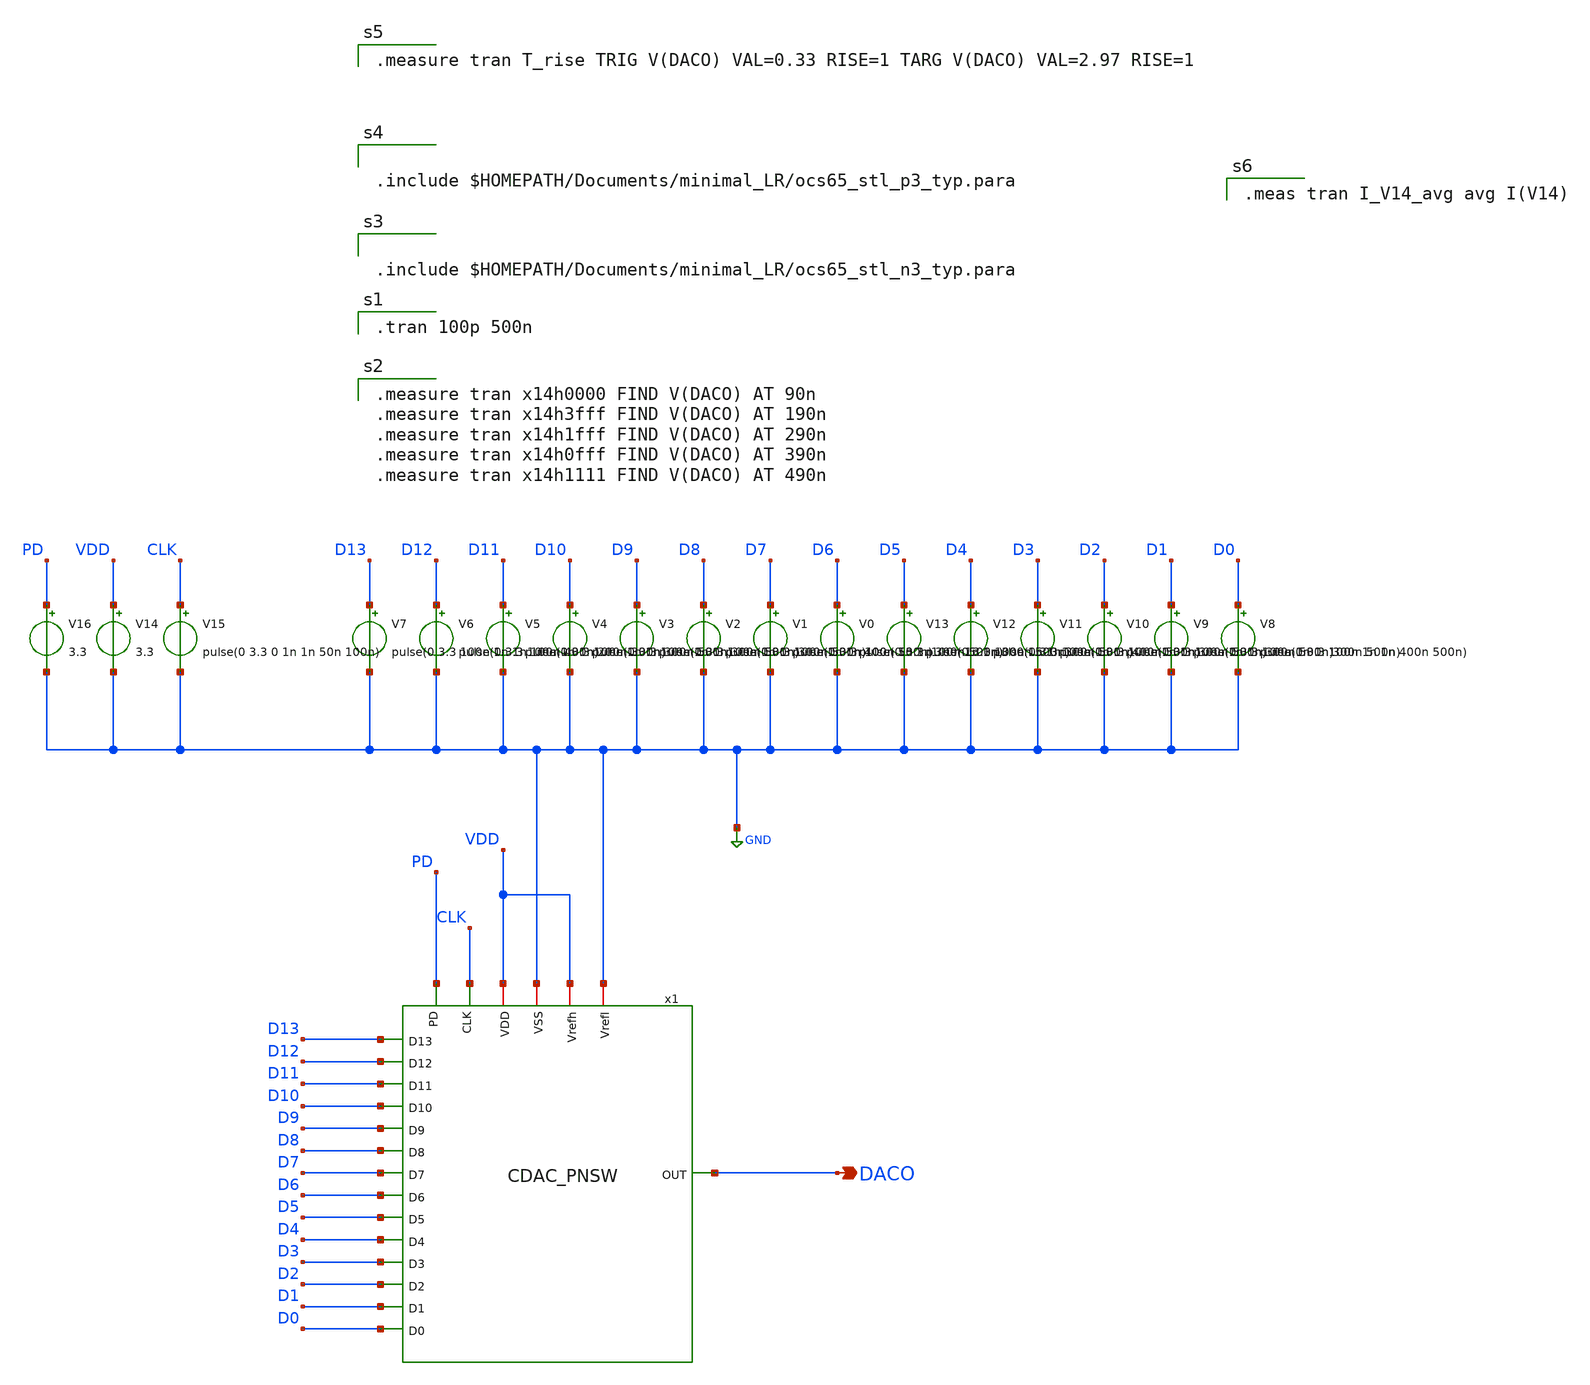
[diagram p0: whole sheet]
** sch_path: CDAC_sim.sch
**.subckt CDAC_sim DACO
*.opin DACO
V14 VDD GND 3.3
V15 CLK GND pulse(0 3.3 0 1n 1n 50n 100n)
V16 PD GND 3.3
V13 D5 GND pulse(0 3.3 100n 1n 1n 300n 500n)
V12 D4 GND pulse(0 3.3 100n 1n 1n 400n 500n)
V11 D3 GND pulse(0 3.3 100n 1n 1n 300n 500n)
V10 D2 GND pulse(0 3.3 100n 1n 1n 300n 500n)
V9 D1 GND pulse(0 3.3 100n 1n 1n 300n 500n)
V8 D0 GND pulse(0 3.3 100n 1n 1n 400n 500n)
V7 D13 GND pulse(0 3.3 100n 1n 1n 100n 400n)
V6 D12 GND pulse(0 3.3 100n 1n 1n 200n 300n)
V5 D11 GND pulse(0 3.3 100n 1n 1n 300n 500n)
V4 D10 GND pulse(0 3.3 100n 1n 1n 300n 500n)
V3 D9 GND pulse(0 3.3 100n 1n 1n 300n 500n)
V2 D8 GND pulse(0 3.3 100n 1n 1n 400n 500n)
V1 D7 GND pulse(0 3.3 100n 1n 1n 300n 500n)
V0 D6 GND pulse(0 3.3 100n 1n 1n 300n 500n)
x1 CLK D11 D13 D12 D7 D10 D1 D0 D9 D8 D2 D6 D5 D4 D3 DACO GND VDD GND VDD PD CDAC_PNSW
**** begin user architecture code

.tran 100p 500n


.measure tran x14h0000 FIND V(DACO) AT 90n
.measure tran x14h3fff FIND V(DACO) AT 190n
.measure tran x14h1fff FIND V(DACO) AT 290n
.measure tran x14h0fff FIND V(DACO) AT 390n
.measure tran x14h1111 FIND V(DACO) AT 490n



.include $HOMEPATH/Documents/minimal_LR/ocs65_stl_n3_typ.para



.include $HOMEPATH/Documents/minimal_LR/ocs65_stl_p3_typ.para


.measure tran T_rise TRIG V(DACO) VAL=0.33 RISE=1 TARG V(DACO) VAL=2.97 RISE=1


.meas tran I_V14_avg avg I(V14)

**** end user architecture code
**.ends

* expanding   symbol:  CDAC_PNSW.sym # of pins=21
** sym_path: CDAC_PNSW.sym
** sch_path: CDAC_PNSW.sch
.subckt CDAC_PNSW CLK D11 D13 D12 D7 D10 D1 D0 D9 D8 D2 D6 D5 D4 D3 OUT VSS VDD Vrefl Vrefh PD
*.opin OUT
*.iopin Vrefh
*.iopin Vrefl
*.ipin D13
*.ipin D12
*.ipin D11
*.ipin D10
*.iopin VSS
*.iopin VDD
*.ipin D9
*.ipin D8
*.ipin D7
*.ipin D6
*.ipin D5
*.ipin D4
*.ipin D3
*.ipin D2
*.ipin D1
*.ipin D0
*.ipin CLK
*.ipin PD
C1 OUT Vrefl 33f m=1
C2 OUT net1 33f m=1
C3 OUT net2 66f m=1
C4 OUT net4 132f m=1
C5 OUT net3 264f m=1
x15 VDD D13b D13 VSS INV
x16 VDD D12b D12 VSS INV
x17 VDD D11b D11 VSS INV
x18 VDD D10b D10 VSS INV
C6 OUT net5 528f m=1
C7 OUT net6 1.056p m=1
C8 OUT net8 2.112p m=1
C9 OUT net7 4.224p m=1
C10 OUT net10 8.448p m=1
C11 OUT net9 16.896p m=1
C12 OUT net11 33.792p m=1
C13 OUT net12 67.584p m=1
C14 OUT net14 135.168p m=1
C15 OUT net13 270.336p m=1
x34 VDD D9b D9 VSS INV
x35 VDD D8b D8 VSS INV
x36 VDD D7b D7 VSS INV
x37 VDD D6b D6 VSS INV
x38 VDD D5b D5 VSS INV
x39 VDD D4b D4 VSS INV
x40 VDD D3b D3 VSS INV
x41 VDD D2b D2 VSS INV
x42 VDD D1b D1 VSS INV
x43 VDD D0b D0 VSS INV
x72 VDD CLK CLK1 VSS net15 NOL
x31 D13bO VSS net13 Vrefl NMOSSW16
x33 D12bO VSS net14 Vrefl NMOSSW8
x29 D11bO VSS net12 Vrefl NMOSSW4
x27 D10bO VSS net11 Vrefl NMOSSW2
x1 resetPD VSS OUT Vrefl NMOSSW16
x2 D0bO VSS net1 Vrefl NMOSSW
x4 D1bO VSS net2 Vrefl NMOSSW
x6 D2bO VSS net4 Vrefl NMOSSW
x8 D3bO VSS net3 Vrefl NMOSSW
x10 D4bO VSS net5 Vrefl NMOSSW
x12 D5bO VSS net6 Vrefl NMOSSW
x14 D6bO VSS net8 Vrefl NMOSSW
x20 D7bO VSS net7 Vrefl NMOSSW
x22 D8bO VSS net10 Vrefl NMOSSW
x24 D9bO VSS net9 Vrefl NMOSSW
x3 D13A net13 Vrefh VDD PMOSSW16
x5 D12A net14 Vrefh VDD PMOSSW8
x7 D11A net12 Vrefh VDD PMOSSW4
x9 D10A net11 Vrefh VDD PMOSSW2
x11 D9A net9 Vrefh VDD PMOSSW
x13 D8A net10 Vrefh VDD PMOSSW
x19 D7A net7 Vrefh VDD PMOSSW
x21 D6A net8 Vrefh VDD PMOSSW
x23 D5A net6 Vrefh VDD PMOSSW
x25 D4A net5 Vrefh VDD PMOSSW
x26 D3A net3 Vrefh VDD PMOSSW
x28 D2A net4 Vrefh VDD PMOSSW
x30 D1A net2 Vrefh VDD PMOSSW
x32 D0A net1 Vrefh VDD PMOSSW
x73 VDD CLK2 net15 VSS INV
x74 VDD net16 PD VSS INV
x75 VDD net17 resetPD net16 VSS OR
x44 VDD D13A CLK1 D13b VSS IMPLY
x45 VDD D12A CLK1 D12b VSS IMPLY
x46 VDD D11A CLK1 D11b VSS IMPLY
x47 VDD D10A CLK1 D10b VSS IMPLY
x48 VDD D9A CLK1 D9b VSS IMPLY
x49 VDD D8A CLK1 D8b VSS IMPLY
x50 VDD D7A CLK1 D7b VSS IMPLY
x51 VDD D6A CLK1 D6b VSS IMPLY
x52 VDD D5A CLK1 D5b VSS IMPLY
x53 VDD D4A CLK1 D4b VSS IMPLY
x54 VDD D3A CLK1 D3b VSS IMPLY
x55 VDD D2A CLK1 D2b VSS IMPLY
x56 VDD D1A CLK1 D1b VSS IMPLY
x57 VDD D0A CLK1 D0b VSS IMPLY
x58 VDD D0bO CLK2 D0b VSS IMPLY
x59 VDD D1bO CLK2 D1b VSS IMPLY
x60 VDD D2bO CLK2 D2b VSS IMPLY
x61 VDD D3bO CLK2 D3b VSS IMPLY
x62 VDD D4bO CLK2 D4b VSS IMPLY
x63 VDD D5bO CLK2 D5b VSS IMPLY
x64 VDD D6bO CLK2 D6b VSS IMPLY
x65 VDD D7bO CLK2 D7b VSS IMPLY
x66 VDD D8bO CLK2 D8b VSS IMPLY
x67 VDD D9bO CLK2 D9b VSS IMPLY
x68 VDD D10bO CLK2 D10b VSS IMPLY
x69 VDD D11bO CLK2 D11b VSS IMPLY
x70 VDD D12bO CLK2 D12b VSS IMPLY
x71 VDD D13bO CLK2 D13b VSS IMPLY
x76 VDD net17 CLK2 VSS INV
.ends


* expanding   symbol:  INV.sym # of pins=4
** sym_path: INV.sym
** sch_path: INV.sch
.subckt INV VDD OUT IN VSS
*.opin OUT
*.ipin IN
*.iopin VDD
*.iopin VSS
M2 OUT IN VDD VDD pch w=5u l=0.35u as=0 ps=0 ad=0 pd=0 m=1
M1 OUT IN VSS VSS nch w=2.5u l=0.35u as=0 ps=0 ad=0 pd=0 m=1
.ends


* expanding   symbol:  NOL.sym # of pins=5
** sym_path: NOL.sym
** sch_path: NOL.sch
.subckt NOL VDD CLK CLK1 VSS CLK2
*.ipin CLK
*.opin CLK1
*.opin CLK2
*.iopin VDD
*.iopin VSS
x3 VDD net1 CLK VSS INV
x1 VDD CLK net9 CLK2 VSS NOR
x2 VDD CLK1 net2 net1 VSS NOR
x4 VDD net3 net2 VSS INV
x5 VDD net4 net3 VSS INV
x6 VDD net5 net4 VSS INV
x7 VDD net17 net5 VSS INV
x8 VDD net6 net9 VSS INV
x9 VDD net7 net6 VSS INV
x10 VDD net8 net7 VSS INV
x11 VDD net13 net8 VSS INV
x12 VDD net10 net13 VSS INV
x13 VDD net11 net10 VSS INV
x14 VDD net12 net11 VSS INV
x15 VDD net32 net12 VSS INV
x16 VDD net14 net17 VSS INV
x17 VDD net15 net14 VSS INV
x18 VDD net16 net15 VSS INV
x19 VDD net33 net16 VSS INV
x20 VDD net18 net33 VSS INV
x21 VDD net19 net18 VSS INV
x22 VDD net20 net19 VSS INV
x23 VDD net24 net20 VSS INV
x24 VDD net21 net24 VSS INV
x25 VDD net22 net21 VSS INV
x26 VDD net23 net22 VSS INV
x27 VDD net34 net23 VSS INV
x28 VDD net25 net32 VSS INV
x29 VDD net26 net25 VSS INV
x30 VDD net27 net26 VSS INV
x31 VDD net31 net27 VSS INV
x32 VDD net28 net31 VSS INV
x33 VDD net29 net28 VSS INV
x34 VDD net30 net29 VSS INV
x35 VDD net50 net30 VSS INV
x36 VDD net35 net34 VSS INV
x37 VDD net36 net35 VSS INV
x38 VDD net37 net36 VSS INV
x39 VDD net41 net37 VSS INV
x40 VDD net38 net41 VSS INV
x41 VDD net39 net38 VSS INV
x42 VDD net40 net39 VSS INV
x43 VDD net42 net40 VSS INV
x44 VDD net43 net50 VSS INV
x45 VDD net44 net43 VSS INV
x46 VDD net45 net44 VSS INV
x47 VDD net49 net45 VSS INV
x48 VDD net46 net49 VSS INV
x49 VDD net47 net46 VSS INV
x50 VDD net48 net47 VSS INV
x51 VDD net61 net48 VSS INV
x52 VDD net51 net42 VSS INV
x53 VDD net53 net51 VSS INV
x54 VDD net52 net61 VSS INV
x55 VDD net60 net52 VSS INV
x56 VDD net54 net53 VSS INV
x57 VDD net55 net54 VSS INV
x58 VDD net56 net55 VSS INV
x59 VDD CLK2 net56 VSS INV
x64 VDD net57 net60 VSS INV
x65 VDD net58 net57 VSS INV
x66 VDD net59 net58 VSS INV
x67 VDD CLK1 net59 VSS INV
.ends


* expanding   symbol:  NMOSSW16.sym # of pins=4
** sym_path: NMOSSW16.sym
** sch_path: NMOSSW16.sch
.subckt NMOSSW16 CLK VSS OUT IN
*.ipin IN
*.opin OUT
*.iopin VSS
*.iopin CLK
x1 CLK VSS OUT IN NMOSSW8
x2 CLK VSS OUT IN NMOSSW8
.ends


* expanding   symbol:  NMOSSW8.sym # of pins=4
** sym_path: NMOSSW8.sym
** sch_path: NMOSSW8.sch
.subckt NMOSSW8 CLK VSS OUT IN
*.ipin IN
*.opin OUT
*.iopin VSS
*.iopin CLK
x1 CLK VSS OUT IN NMOSSW4
x2 CLK VSS OUT IN NMOSSW4
.ends


* expanding   symbol:  NMOSSW4.sym # of pins=4
** sym_path: NMOSSW4.sym
** sch_path: NMOSSW4.sch
.subckt NMOSSW4 CLK VSS OUT IN
*.ipin IN
*.opin OUT
*.iopin VSS
*.iopin CLK
x1 CLK VSS OUT IN NMOSSW2
x2 CLK VSS OUT IN NMOSSW2
.ends


* expanding   symbol:  NMOSSW2.sym # of pins=4
** sym_path: NMOSSW2.sym
** sch_path: NMOSSW2.sch
.subckt NMOSSW2 CLK VSS OUT IN
*.ipin IN
*.opin OUT
*.iopin VSS
*.iopin CLK
x1 CLK VSS OUT IN NMOSSW
x2 CLK VSS OUT IN NMOSSW
.ends


* expanding   symbol:  NMOSSW.sym # of pins=4
** sym_path: NMOSSW.sym
** sch_path: NMOSSW.sch
.subckt NMOSSW CLK VSS OUT IN
*.ipin IN
*.iopin VSS
*.opin OUT
*.iopin CLK
M1 OUT CLK IN VSS nch w=25u l=0.35u as=0 ps=0 ad=0 pd=0 m=1
.ends


* expanding   symbol:  PMOSSW16.sym # of pins=4
** sym_path: PMOSSW16.sym
** sch_path: PMOSSW16.sch
.subckt PMOSSW16 CLK OUT IN VDD
*.ipin IN
*.opin OUT
*.iopin CLK
*.iopin VDD
x1 CLK OUT IN VDD PMOSSW8
x2 CLK OUT IN VDD PMOSSW8
.ends


* expanding   symbol:  PMOSSW8.sym # of pins=4
** sym_path: PMOSSW8.sym
** sch_path: PMOSSW8.sch
.subckt PMOSSW8 CLK OUT IN VDD
*.ipin IN
*.opin OUT
*.iopin CLK
*.iopin VDD
x1 CLK OUT IN VDD PMOSSW4
x2 CLK OUT IN VDD PMOSSW4
.ends


* expanding   symbol:  PMOSSW4.sym # of pins=4
** sym_path: PMOSSW4.sym
** sch_path: PMOSSW4.sch
.subckt PMOSSW4 CLK OUT IN VDD
*.ipin IN
*.opin OUT
*.iopin CLK
*.iopin VDD
x1 CLK OUT IN VDD PMOSSW2
x2 CLK OUT IN VDD PMOSSW2
.ends


* expanding   symbol:  PMOSSW2.sym # of pins=4
** sym_path: PMOSSW2.sym
** sch_path: PMOSSW2.sch
.subckt PMOSSW2 CLK OUT IN VDD
*.ipin IN
*.opin OUT
*.iopin CLK
*.iopin VDD
x1 CLK OUT IN VDD PMOSSW
x2 CLK OUT IN VDD PMOSSW
.ends


* expanding   symbol:  PMOSSW.sym # of pins=4
** sym_path: PMOSSW.sym
** sch_path: PMOSSW.sch
.subckt PMOSSW CLK OUT IN VDD
*.ipin IN
*.opin OUT
*.iopin VDD
*.iopin CLK
M5 OUT CLK IN VDD pch w=25u l=0.35u as=0 ps=0 ad=0 pd=0 m=1
.ends


* expanding   symbol:  OR.sym # of pins=5
** sym_path: OR.sym
** sch_path: OR.sch
.subckt OR VDD A Y B VSS
*.iopin VDD
*.ipin A
*.ipin B
*.iopin VSS
*.opin Y
M1 net1 A VSS VSS nch w=3.5u l=0.35u as=0 ps=0 ad=0 pd=0 m=1
M2 net2 A VDD VDD pch w=3.5u l=0.35u as=0 ps=0 ad=0 pd=0 m=1
M3 net1 B net2 VDD pch w=3.5u l=0.35u as=0 ps=0 ad=0 pd=0 m=1
M4 net1 B VSS VSS nch w=3.5u l=0.35u as=0 ps=0 ad=0 pd=0 m=1
M5 Y net1 VDD VDD pch w=10u l=0.35u as=0 ps=0 ad=0 pd=0 m=1
M6 Y net1 VSS VSS nch w=5u l=0.35u as=0 ps=0 ad=0 pd=0 m=1
.ends


* expanding   symbol:  IMPLY.sym # of pins=5
** sym_path: IMPLY.sym
** sch_path: IMPLY.sch
.subckt IMPLY VDD Y A B VSS
*.ipin A
*.ipin B
*.iopin VDD
*.iopin VSS
*.opin Y
x2 VDD net1 A VSS INV
x1 VDD net1 Y B VSS OR
.ends


* expanding   symbol:  NOR.sym # of pins=5
** sym_path: NOR.sym
** sch_path: NOR.sch
.subckt NOR VDD A Y B VSS
*.iopin VDD
*.ipin A
*.ipin B
*.iopin VSS
*.opin Y
M1 Y A VSS VSS nch w=3.5u l=0.35u as=0 ps=0 ad=0 pd=0 m=1
M2 net1 A VDD VDD pch w=3.5u l=0.35u as=0 ps=0 ad=0 pd=0 m=1
M3 Y B net1 VDD pch w=3.5u l=0.35u as=0 ps=0 ad=0 pd=0 m=1
M4 Y B VSS VSS nch w=3.5u l=0.35u as=0 ps=0 ad=0 pd=0 m=1
.ends

.GLOBAL GND
.end
